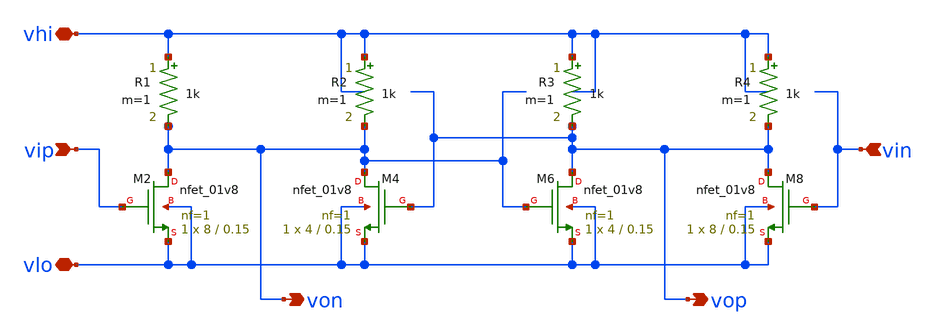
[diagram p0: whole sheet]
** sch_path: xschem/xcpinv_res_cell.sch
**.subckt xcpinv_res_cell vhi vlo vip vin von vop
*.iopin vhi
*.iopin vlo
*.ipin vip
*.ipin vin
*.opin von
*.opin vop
XM2 von vip vlo vlo sky130_fd_pr__nfet_01v8 L=0.15 W=8 nf=1 ad='int((nf+1)/2) * W/nf * 0.29' as='int((nf+2)/2) * W/nf * 0.29'
+ pd='2*int((nf+1)/2) * (W/nf + 0.29)' ps='2*int((nf+2)/2) * (W/nf + 0.29)' nrd='0.29 / W' nrs='0.29 / W'
+ sa=0 sb=0 sd=0 mult=1 m=1
XM4 von vop vlo vlo sky130_fd_pr__nfet_01v8 L=0.15 W=4 nf=1 ad='int((nf+1)/2) * W/nf * 0.29' as='int((nf+2)/2) * W/nf * 0.29'
+ pd='2*int((nf+1)/2) * (W/nf + 0.29)' ps='2*int((nf+2)/2) * (W/nf + 0.29)' nrd='0.29 / W' nrs='0.29 / W'
+ sa=0 sb=0 sd=0 mult=1 m=1
XM6 vop von vlo vlo sky130_fd_pr__nfet_01v8 L=0.15 W=4 nf=1 ad='int((nf+1)/2) * W/nf * 0.29' as='int((nf+2)/2) * W/nf * 0.29'
+ pd='2*int((nf+1)/2) * (W/nf + 0.29)' ps='2*int((nf+2)/2) * (W/nf + 0.29)' nrd='0.29 / W' nrs='0.29 / W'
+ sa=0 sb=0 sd=0 mult=1 m=1
XM8 vop vin vlo vlo sky130_fd_pr__nfet_01v8 L=0.15 W=8 nf=1 ad='int((nf+1)/2) * W/nf * 0.29' as='int((nf+2)/2) * W/nf * 0.29'
+ pd='2*int((nf+1)/2) * (W/nf + 0.29)' ps='2*int((nf+2)/2) * (W/nf + 0.29)' nrd='0.29 / W' nrs='0.29 / W'
+ sa=0 sb=0 sd=0 mult=1 m=1
R1 vhi von 1k m=1
R2 vhi von 1k m=1
R3 vhi vop 1k m=1
R4 vhi vop 1k m=1
**.ends
.end
